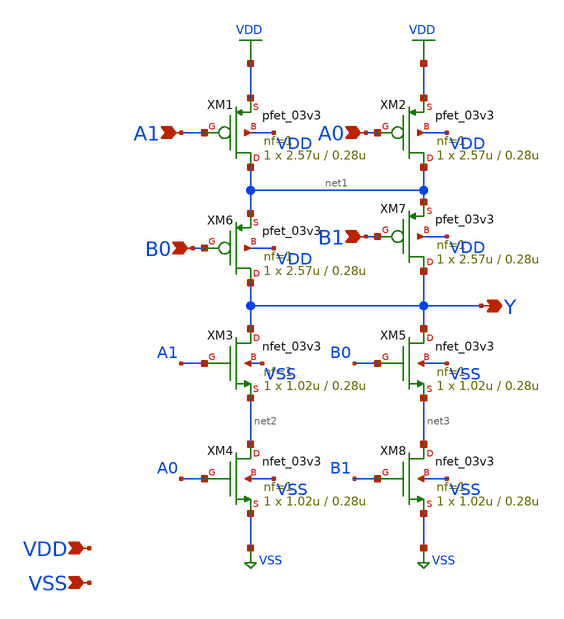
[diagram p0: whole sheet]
** sch_path: xschem/gf180mcu_ocd_sc_rt12t3v3__aoi22_1.sch
**.subckt gf180mcu_ocd_sc_rt12t3v3__aoi22_1 A1 A0 B0 B1 Y VDD VSS
*.ipin A1
*.ipin A0
*.ipin B0
*.ipin B1
*.opin Y
*.ipin VDD
*.ipin VSS
XM1 net1 A1 VDD VDD pfet_03v3 L=0.28u W=2.57u nf=1 ad='int((nf+1)/2) * W/nf * 0.18u' as='int((nf+2)/2) * W/nf * 0.18u'
+ pd='2*int((nf+1)/2) * (W/nf + 0.18u)' ps='2*int((nf+2)/2) * (W/nf + 0.18u)' nrd='0.18u / W' nrs='0.18u / W'
+ sa=0 sb=0 sd=0 m=1
XM2 net1 A0 VDD VDD pfet_03v3 L=0.28u W=2.57u nf=1 ad='int((nf+1)/2) * W/nf * 0.18u' as='int((nf+2)/2) * W/nf * 0.18u'
+ pd='2*int((nf+1)/2) * (W/nf + 0.18u)' ps='2*int((nf+2)/2) * (W/nf + 0.18u)' nrd='0.18u / W' nrs='0.18u / W'
+ sa=0 sb=0 sd=0 m=1
XM3 Y A1 net2 VSS nfet_03v3 L=0.28u W=1.02u nf=1 ad='int((nf+1)/2) * W/nf * 0.18u' as='int((nf+2)/2) * W/nf * 0.18u'
+ pd='2*int((nf+1)/2) * (W/nf + 0.18u)' ps='2*int((nf+2)/2) * (W/nf + 0.18u)' nrd='0.18u / W' nrs='0.18u / W'
+ sa=0 sb=0 sd=0 m=1
XM4 net2 A0 VSS VSS nfet_03v3 L=0.28u W=1.02u nf=1 ad='int((nf+1)/2) * W/nf * 0.18u' as='int((nf+2)/2) * W/nf * 0.18u'
+ pd='2*int((nf+1)/2) * (W/nf + 0.18u)' ps='2*int((nf+2)/2) * (W/nf + 0.18u)' nrd='0.18u / W' nrs='0.18u / W'
+ sa=0 sb=0 sd=0 m=1
XM5 Y B0 net3 VSS nfet_03v3 L=0.28u W=1.02u nf=1 ad='int((nf+1)/2) * W/nf * 0.18u' as='int((nf+2)/2) * W/nf * 0.18u'
+ pd='2*int((nf+1)/2) * (W/nf + 0.18u)' ps='2*int((nf+2)/2) * (W/nf + 0.18u)' nrd='0.18u / W' nrs='0.18u / W'
+ sa=0 sb=0 sd=0 m=1
XM6 Y B0 net1 VDD pfet_03v3 L=0.28u W=2.57u nf=1 ad='int((nf+1)/2) * W/nf * 0.18u' as='int((nf+2)/2) * W/nf * 0.18u'
+ pd='2*int((nf+1)/2) * (W/nf + 0.18u)' ps='2*int((nf+2)/2) * (W/nf + 0.18u)' nrd='0.18u / W' nrs='0.18u / W'
+ sa=0 sb=0 sd=0 m=1
XM7 Y B1 net1 VDD pfet_03v3 L=0.28u W=2.57u nf=1 ad='int((nf+1)/2) * W/nf * 0.18u' as='int((nf+2)/2) * W/nf * 0.18u'
+ pd='2*int((nf+1)/2) * (W/nf + 0.18u)' ps='2*int((nf+2)/2) * (W/nf + 0.18u)' nrd='0.18u / W' nrs='0.18u / W'
+ sa=0 sb=0 sd=0 m=1
XM8 net3 B1 VSS VSS nfet_03v3 L=0.28u W=1.02u nf=1 ad='int((nf+1)/2) * W/nf * 0.18u' as='int((nf+2)/2) * W/nf * 0.18u'
+ pd='2*int((nf+1)/2) * (W/nf + 0.18u)' ps='2*int((nf+2)/2) * (W/nf + 0.18u)' nrd='0.18u / W' nrs='0.18u / W'
+ sa=0 sb=0 sd=0 m=1
**.ends
.GLOBAL VDD
.GLOBAL VSS
.end
